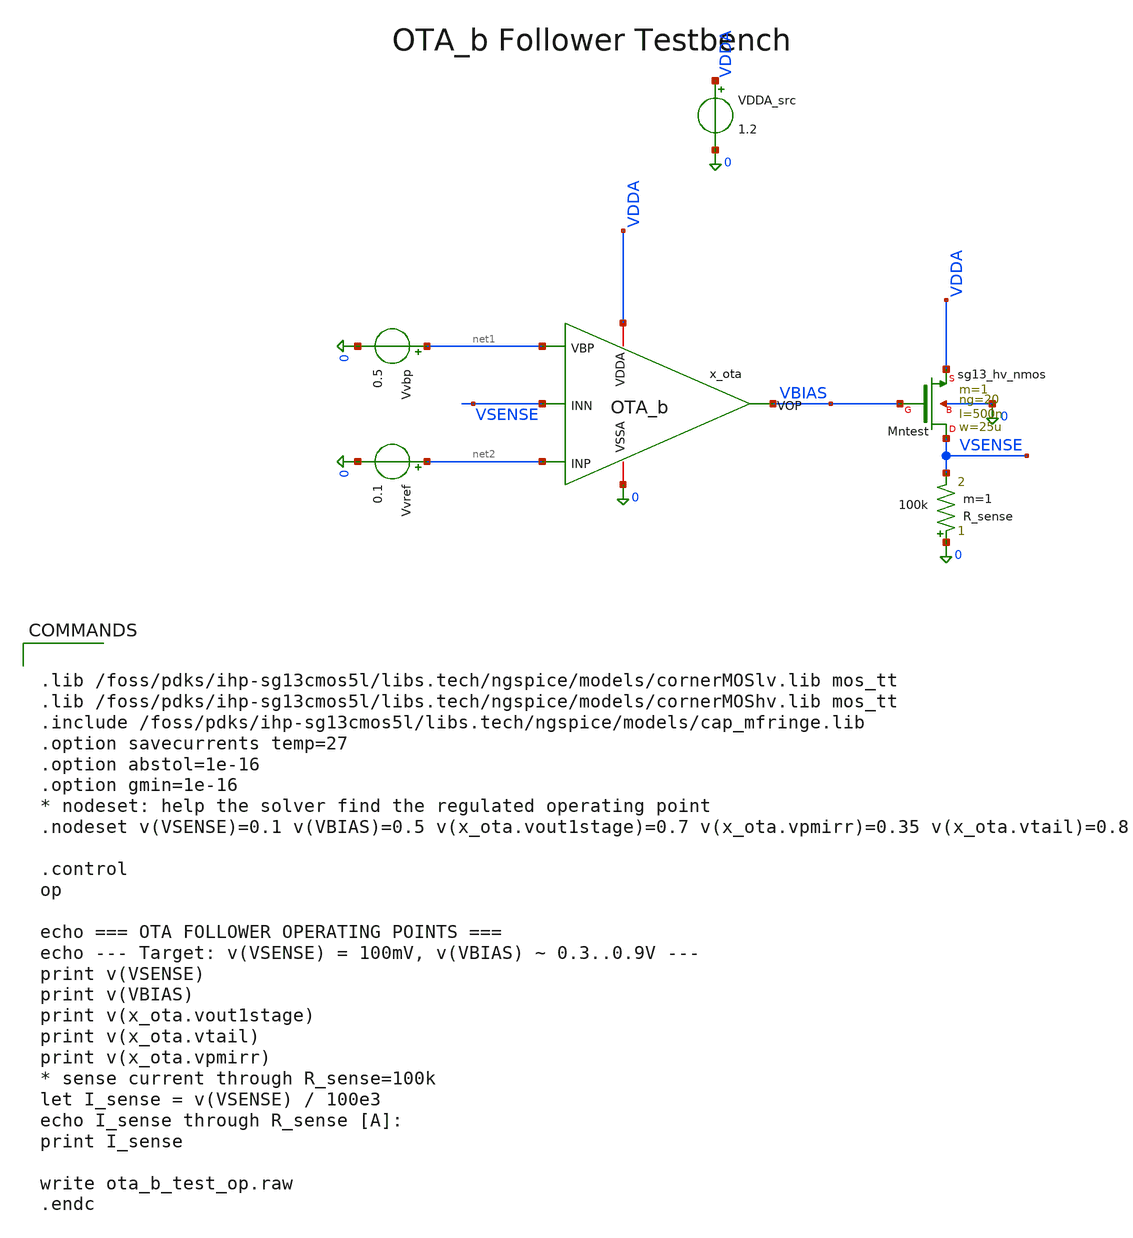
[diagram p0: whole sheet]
** sch_path: OTA_b_test.sch
**.subckt OTA_b_test
x_ota VDDA net1 VSENSE net2 VBIAS 0 OTA_b
XMntest VSENSE VBIAS VDDA 0 sg13_hv_nmos w=25u l=500n ng=20 m=1 mm_ok=1
R_sense 0 VSENSE 100k m=1
Vvbp net1 0 0.5
Vvref net2 0 0.1
VDDA_src VDDA 0 1.2
**** begin user architecture code


.lib /foss/pdks/ihp-sg13cmos5l/libs.tech/ngspice/models/cornerMOSlv.lib mos_tt
.lib /foss/pdks/ihp-sg13cmos5l/libs.tech/ngspice/models/cornerMOShv.lib mos_tt
.include /foss/pdks/ihp-sg13cmos5l/libs.tech/ngspice/models/cap_mfringe.lib
.option savecurrents temp=27
.option abstol=1e-16
.option gmin=1e-16
* nodeset: help the solver find the regulated operating point
.nodeset v(VSENSE)=0.1 v(VBIAS)=0.5 v(x_ota.vout1stage)=0.7 v(x_ota.vpmirr)=0.35 v(x_ota.vtail)=0.8

.control
op

echo === OTA FOLLOWER OPERATING POINTS ===
echo --- Target: v(VSENSE) = 100mV, v(VBIAS) ~ 0.3..0.9V ---
print v(VSENSE)
print v(VBIAS)
print v(x_ota.vout1stage)
print v(x_ota.vtail)
print v(x_ota.vpmirr)
* sense current through R_sense=100k
let I_sense = v(VSENSE) / 100e3
echo I_sense through R_sense [A]:
print I_sense

write ota_b_test_op.raw
.endc


**** end user architecture code
**.ends
.end
